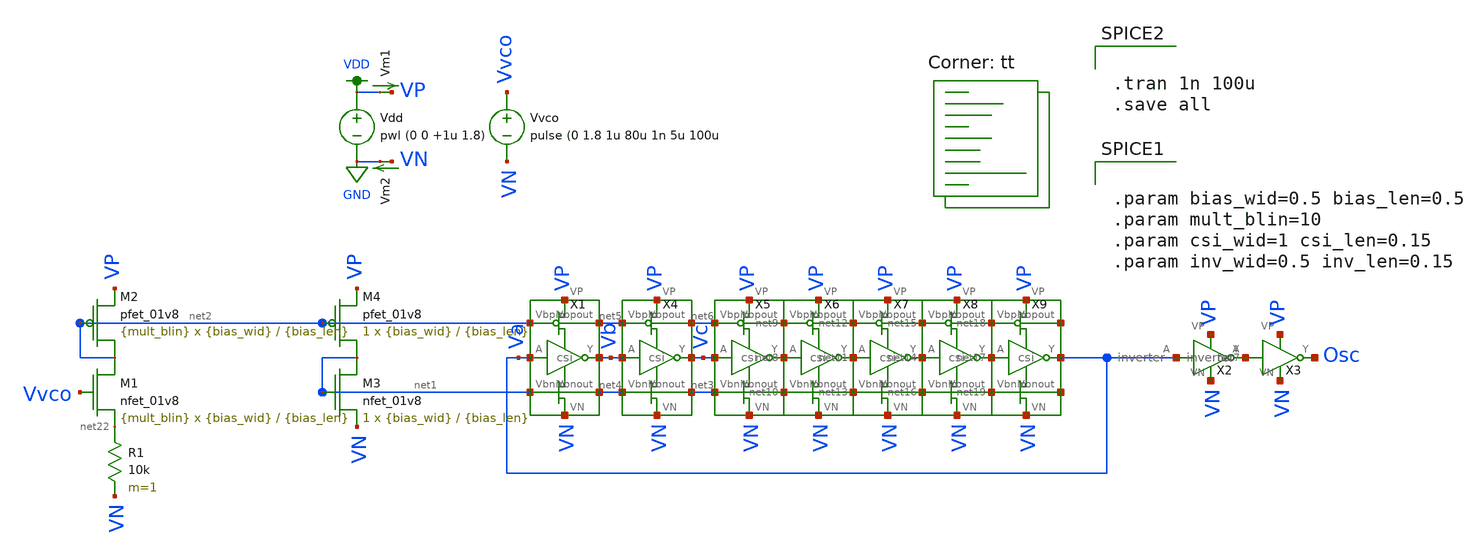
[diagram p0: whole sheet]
** sch_path: test_vco.sch
**.subckt test_vco
X1 VP VN Va Vb net2 net1 net5 net4 csi
X2 Va net7 VP VN inverter
X3 net7 Osc VP VN inverter
XM3 net1 net1 VN VN sky130_fd_pr__nfet_01v8 L={bias_len} W={bias_wid} nf=1 ad='int((nf+1)/2) * W/nf * 0.29'
+ as='int((nf+2)/2) * W/nf * 0.29' pd='2*int((nf+1)/2) * (W/nf + 0.29)' ps='2*int((nf+2)/2) * (W/nf + 0.29)'
+ nrd='0.29 / W' nrs='0.29 / W' sa=0 sb=0 sd=0 mult=1 m=1
XM4 net1 net2 VP VP sky130_fd_pr__pfet_01v8 L={bias_len} W={bias_wid} nf=1 ad='int((nf+1)/2) * W/nf * 0.29'
+ as='int((nf+2)/2) * W/nf * 0.29' pd='2*int((nf+1)/2) * (W/nf + 0.29)' ps='2*int((nf+2)/2) * (W/nf + 0.29)'
+ nrd='0.29 / W' nrs='0.29 / W' sa=0 sb=0 sd=0 mult=1 m=1
X4 VP VN Vb Vc net5 net4 net6 net3 csi
X5 VP VN Vc net8 net6 net3 net9 net10 csi
Vdd VDD GND pwl (0 0 +1u 1.8)
Vm1 VDD VP 0
.save i(vm1)
Vm2 VN GND 0
.save i(vm2)
Vvco Vvco VN pulse (0 1.8 1u 80u 1n 5u 100u
X6 VP VN net8 net11 net9 net10 net12 net13 csi
X7 VP VN net11 net14 net12 net13 net15 net16 csi
X8 VP VN net14 net17 net15 net16 net18 net19 csi
X9 VP VN net17 Va net18 net19 net20 net21 csi
R1 net22 VN 10k m=1
XM1 net2 Vvco net22 VN sky130_fd_pr__nfet_01v8 L={bias_len} W={bias_wid} nf=1 ad='int((nf+1)/2) * W/nf * 0.29'
+ as='int((nf+2)/2) * W/nf * 0.29' pd='2*int((nf+1)/2) * (W/nf + 0.29)' ps='2*int((nf+2)/2) * (W/nf + 0.29)'
+ nrd='0.29 / W' nrs='0.29 / W' sa=0 sb=0 sd=0 mult={mult_blin} m={mult_blin}
XM2 net2 net2 VP VP sky130_fd_pr__pfet_01v8 L={bias_len} W={bias_wid} nf=1 ad='int((nf+1)/2) * W/nf * 0.29'
+ as='int((nf+2)/2) * W/nf * 0.29' pd='2*int((nf+1)/2) * (W/nf + 0.29)' ps='2*int((nf+2)/2) * (W/nf + 0.29)'
+ nrd='0.29 / W' nrs='0.29 / W' sa=0 sb=0 sd=0 mult={mult_blin} m={mult_blin}
**** begin user architecture code


.tran 1n 100u
.save all




.param bias_wid=0.5 bias_len=0.5
.param mult_blin=10
.param csi_wid=1 csi_len=0.15
.param inv_wid=0.5 inv_len=0.15


.lib $::SKYWATER_MODELS/sky130.lib.spice tt
**** end user architecture code
**.ends

* expanding   symbol:  csi.sym # of pins=8
** sym_path: csi.sym
** sch_path: csi.sch
.subckt csi VP VN A Y Vbpin Vbnin Vbpout Vbnout
*.iopin VN
*.iopin VP
*.opin Y
*.ipin Vbpin
*.ipin A
*.ipin Vbnin
*.opin Vbpout
*.opin Vbnout
XM1 Y A net1 VN sky130_fd_pr__nfet_01v8 L={csi_len} W={csi_wid} nf=1 ad='int((nf+1)/2) * W/nf * 0.29'
+ as='int((nf+2)/2) * W/nf * 0.29' pd='2*int((nf+1)/2) * (W/nf + 0.29)' ps='2*int((nf+2)/2) * (W/nf + 0.29)'
+ nrd='0.29 / W' nrs='0.29 / W' sa=0 sb=0 sd=0 mult=1 m=1
XM2 Y A net2 VP sky130_fd_pr__pfet_01v8 L={csi_len} W={csi_wid} nf=1 ad='int((nf+1)/2) * W/nf * 0.29'
+ as='int((nf+2)/2) * W/nf * 0.29' pd='2*int((nf+1)/2) * (W/nf + 0.29)' ps='2*int((nf+2)/2) * (W/nf + 0.29)'
+ nrd='0.29 / W' nrs='0.29 / W' sa=0 sb=0 sd=0 mult=1 m=1
XM3 net1 Vbnin VN VN sky130_fd_pr__nfet_01v8 L={bias_len} W={bias_wid} nf=1 ad='int((nf+1)/2) * W/nf * 0.29'
+ as='int((nf+2)/2) * W/nf * 0.29' pd='2*int((nf+1)/2) * (W/nf + 0.29)' ps='2*int((nf+2)/2) * (W/nf + 0.29)'
+ nrd='0.29 / W' nrs='0.29 / W' sa=0 sb=0 sd=0 mult=1 m=1
XM4 net2 Vbpin VP VP sky130_fd_pr__pfet_01v8 L={bias_len} W={bias_wid} nf=1 ad='int((nf+1)/2) * W/nf * 0.29'
+ as='int((nf+2)/2) * W/nf * 0.29' pd='2*int((nf+1)/2) * (W/nf + 0.29)' ps='2*int((nf+2)/2) * (W/nf + 0.29)'
+ nrd='0.29 / W' nrs='0.29 / W' sa=0 sb=0 sd=0 mult=1 m=1
Vm1 Vbpin Vbpout 0
.save i(vm1)
Vm2 Vbnin Vbnout 0
.save i(vm2)
.ends


* expanding   symbol:  inverter.sym # of pins=4
** sym_path: inverter.sym
** sch_path: inverter.sch
.subckt inverter A Y VP VN
*.iopin VP
*.ipin A
*.opin Y
*.iopin VN
XM2 Y A VP VP sky130_fd_pr__pfet_01v8 L={inv_len} W={inv_wid} nf=1 ad='int((nf+1)/2) * W/nf * 0.29' as='int((nf+2)/2) * W/nf * 0.29'
+ pd='2*int((nf+1)/2) * (W/nf + 0.29)' ps='2*int((nf+2)/2) * (W/nf + 0.29)' nrd='0.29 / W' nrs='0.29 / W'
+ sa=0 sb=0 sd=0 mult=1 m=1
XM1 Y A VN VN sky130_fd_pr__nfet_01v8 L={inv_len} W={inv_wid} nf=1 ad='int((nf+1)/2) * W/nf * 0.29' as='int((nf+2)/2) * W/nf * 0.29'
+ pd='2*int((nf+1)/2) * (W/nf + 0.29)' ps='2*int((nf+2)/2) * (W/nf + 0.29)' nrd='0.29 / W' nrs='0.29 / W'
+ sa=0 sb=0 sd=0 mult=1 m=1
.ends

.GLOBAL GND
.GLOBAL VDD
.end
